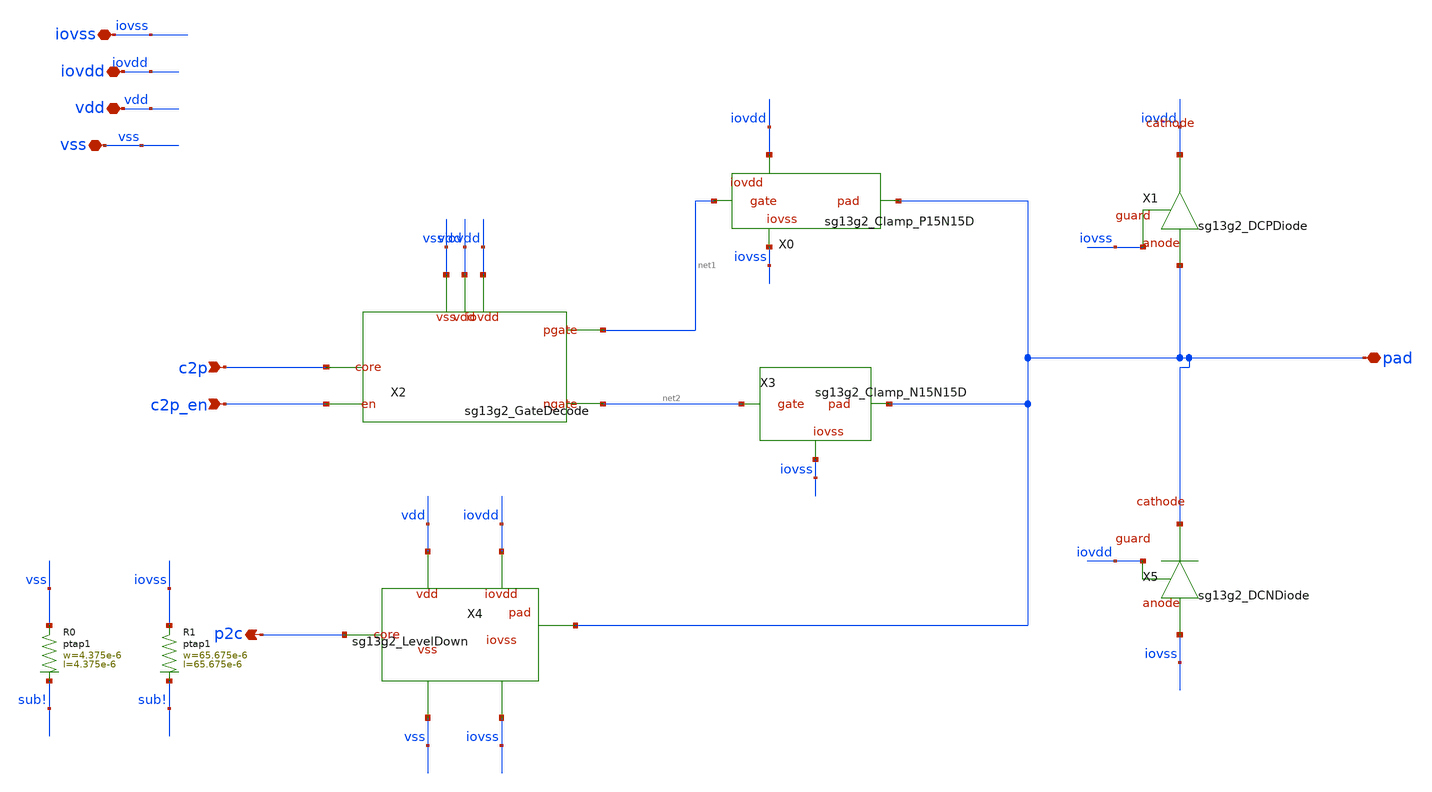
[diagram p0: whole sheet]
** sch_path: ihp-sg13g2/libs.ref/sg13g2_io/sch/xschem/sg13g2_IOPadInOut30mA.sch
**.subckt sg13g2_IOPadInOut30mA vdd vss iovdd c2p c2p_en pad iovss p2c
*.iopin vdd
*.iopin vss
*.iopin iovdd
*.ipin c2p
*.ipin c2p_en
*.iopin pad
*.iopin iovss
*.opin p2c
X0 pad net1 iovss iovdd sg13g2_Clamp_P15N15D
X1 iovss iovdd pad sg13g2_DCPDiode
X2 c2p_en c2p net1 net2 vss vdd iovdd sg13g2_GateDecode
X3 pad net2 iovss sg13g2_Clamp_N15N15D
X4 p2c vss vdd pad iovss iovdd sg13g2_LevelDown
X5 iovdd pad iovss sg13g2_DCNDiode
XR0 vss sub! ptap1 R=26.75 w=4.375e-6 l=4.375e-6
XR1 iovss sub! ptap1 R=214.2m w=65.675e-6 l=65.675e-6
**.ends
.end
